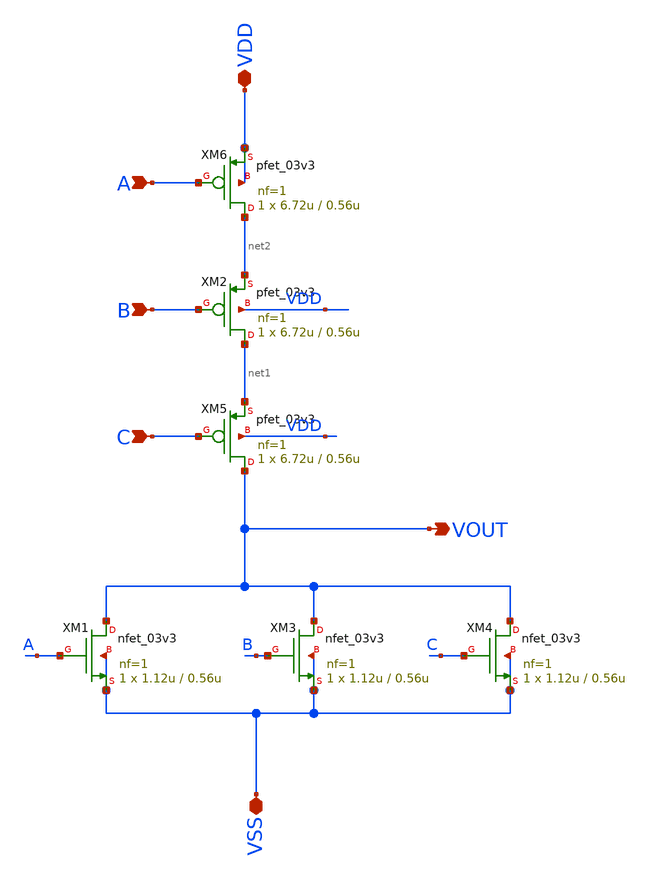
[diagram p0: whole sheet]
** sch_path: PLL-main/schematic/xschem/3_inp_NOR.sch
* Copyright 2022 GlobalFoundries PDK Authors
* Licensed under the Apache License, Version 2.0 (the "License");
* you may not use this file except in compliance with the License.
* You may obtain a copy of the License at
* https://www.apache.org/licenses/LICENSE-2.0
* Unless required by applicable law or agreed to in writing, software
* distributed under the License is distributed on an "AS IS" BASIS,
* WITHOUT WARRANTIES OR CONDITIONS OF ANY KIND, either express or implied.
* See the License for the specific language governing permissions and
* limitations under the License.
**.subckt 3_inp_NOR VSS VDD A B C VOUT
*.iopin VSS
*.iopin VDD
*.ipin A
*.ipin B
*.ipin C
*.opin VOUT
XM1 VOUT A VSS VSS nfet_03v3 L=0.56u W=1.12u nf=1 ad='int((nf+1)/2) * W/nf * 0.18u' as='int((nf+2)/2) * W/nf * 0.18u'
+ pd='2*int((nf+1)/2) * (W/nf + 0.18u)' ps='2*int((nf+2)/2) * (W/nf + 0.18u)' nrd='0.18u / W' nrs='0.18u / W'
+ sa=0 sb=0 sd=0 m=1
XM2 net1 B net2 VDD pfet_03v3 L=0.56u W=6.72u nf=1 ad='int((nf+1)/2) * W/nf * 0.18u' as='int((nf+2)/2) * W/nf * 0.18u'
+ pd='2*int((nf+1)/2) * (W/nf + 0.18u)' ps='2*int((nf+2)/2) * (W/nf + 0.18u)' nrd='0.18u / W' nrs='0.18u / W'
+ sa=0 sb=0 sd=0 m=1
XM3 VOUT B VSS VSS nfet_03v3 L=0.56u W=1.12u nf=1 ad='int((nf+1)/2) * W/nf * 0.18u' as='int((nf+2)/2) * W/nf * 0.18u'
+ pd='2*int((nf+1)/2) * (W/nf + 0.18u)' ps='2*int((nf+2)/2) * (W/nf + 0.18u)' nrd='0.18u / W' nrs='0.18u / W'
+ sa=0 sb=0 sd=0 m=1
XM4 VOUT C VSS VSS nfet_03v3 L=0.56u W=1.12u nf=1 ad='int((nf+1)/2) * W/nf * 0.18u' as='int((nf+2)/2) * W/nf * 0.18u'
+ pd='2*int((nf+1)/2) * (W/nf + 0.18u)' ps='2*int((nf+2)/2) * (W/nf + 0.18u)' nrd='0.18u / W' nrs='0.18u / W'
+ sa=0 sb=0 sd=0 m=1
XM5 VOUT C net1 VDD pfet_03v3 L=0.56u W=6.72u nf=1 ad='int((nf+1)/2) * W/nf * 0.18u' as='int((nf+2)/2) * W/nf * 0.18u'
+ pd='2*int((nf+1)/2) * (W/nf + 0.18u)' ps='2*int((nf+2)/2) * (W/nf + 0.18u)' nrd='0.18u / W' nrs='0.18u / W'
+ sa=0 sb=0 sd=0 m=1
XM6 net2 A VDD VDD pfet_03v3 L=0.56u W=6.72u nf=1 ad='int((nf+1)/2) * W/nf * 0.18u' as='int((nf+2)/2) * W/nf * 0.18u'
+ pd='2*int((nf+1)/2) * (W/nf + 0.18u)' ps='2*int((nf+2)/2) * (W/nf + 0.18u)' nrd='0.18u / W' nrs='0.18u / W'
+ sa=0 sb=0 sd=0 m=1
**.ends
.end
